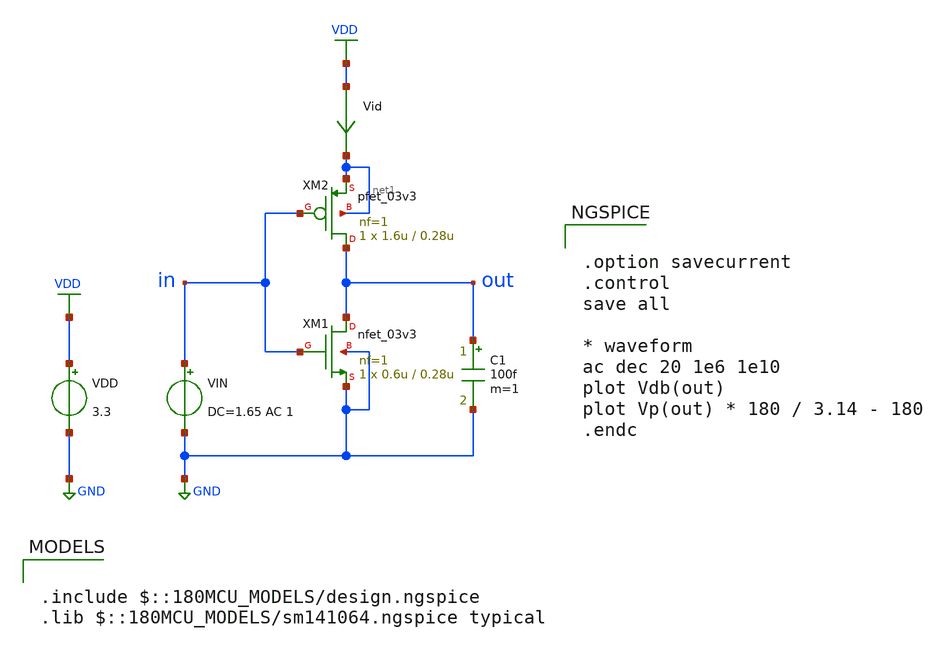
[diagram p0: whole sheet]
** sch_path: fifty_nifty/01_inv_ac.sch
**.subckt 01_inv_ac
XM1 out in GND GND nfet_03v3 L=0.28u W=0.6u nf=1 ad='int((nf+1)/2) * W/nf * 0.18u' as='int((nf+2)/2) * W/nf * 0.18u'
+ pd='2*int((nf+1)/2) * (W/nf + 0.18u)' ps='2*int((nf+2)/2) * (W/nf + 0.18u)' nrd='0.18u / W' nrs='0.18u / W'
+ sa=0 sb=0 sd=0 m=1
VIN in GND DC=1.65 AC 1
Vid VDD net1 0
.save i(vid)
XM2 out in net1 net1 pfet_03v3 L=0.28u W=1.6u nf=1 ad='int((nf+1)/2) * W/nf * 0.18u' as='int((nf+2)/2) * W/nf * 0.18u'
+ pd='2*int((nf+1)/2) * (W/nf + 0.18u)' ps='2*int((nf+2)/2) * (W/nf + 0.18u)' nrd='0.18u / W' nrs='0.18u / W'
+ sa=0 sb=0 sd=0 m=1
VDD VDD GND 3.3
C1 out GND 100f m=1
**** begin user architecture code

.option savecurrent
.control
save all

* waveform
ac dec 20 1e6 1e10
plot Vdb(out)
plot Vp(out) * 180 / 3.14 - 180
.endc


.include $::180MCU_MODELS/design.ngspice
.lib $::180MCU_MODELS/sm141064.ngspice typical

**** end user architecture code
**.ends
.GLOBAL GND
.GLOBAL VDD
.end
